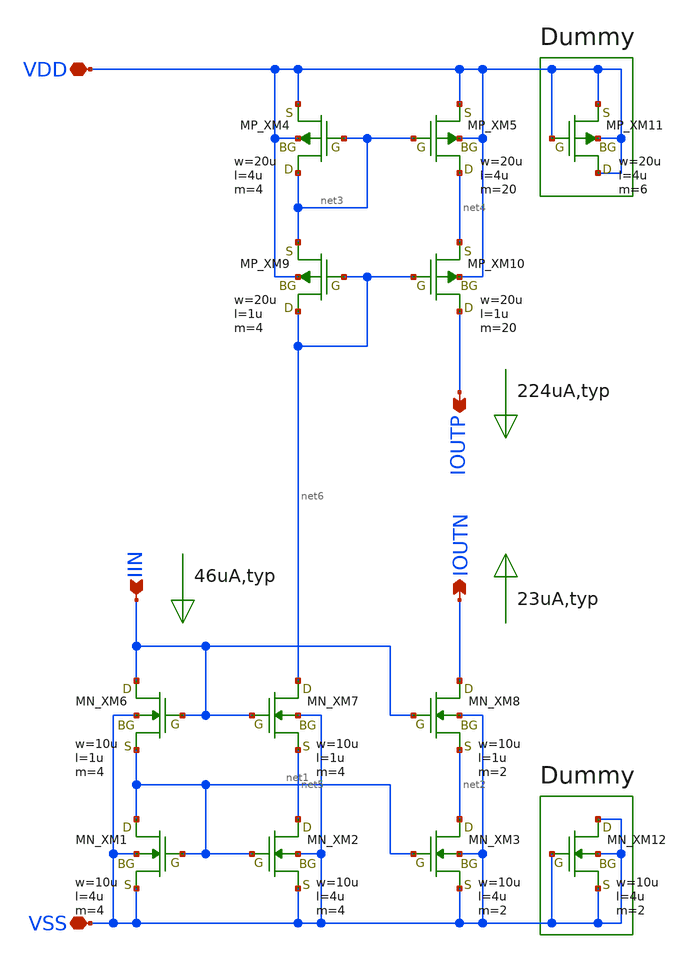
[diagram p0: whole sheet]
** sch_path: member_project/BGR/Maehashi/design/ibuf.sch
**.subckt ibuf VSS VDD IIN IOUTN IOUTP
*.iopin VSS
*.iopin VDD
*.ipin IIN
*.opin IOUTN
*.opin IOUTP
XXM1 net1 net1 VSS VSS NMOS w=10u l=4u as=0 ad=0 ps=0 pd=0 nrd=0 nrs=0 m=4
XXM2 net5 net1 VSS VSS NMOS w=10u l=4u as=0 ad=0 ps=0 pd=0 nrd=0 nrs=0 m=4
XXM3 net2 net1 VSS VSS NMOS w=10u l=4u as=0 ad=0 ps=0 pd=0 nrd=0 nrs=0 m=2
XXM4 net3 net3 VDD VDD PMOS w=20u l=4u as=0 ad=0 ps=0 pd=0 nrd=0 nrs=0 m=4
XXM5 net4 net3 VDD VDD PMOS w=20u l=4u as=0 ad=0 ps=0 pd=0 nrd=0 nrs=0 m=20
XXM6 IIN IIN net1 VSS NMOS w=10u l=1u as=0 ad=0 ps=0 pd=0 nrd=0 nrs=0 m=4
XXM7 net6 IIN net5 VSS NMOS w=10u l=1u as=0 ad=0 ps=0 pd=0 nrd=0 nrs=0 m=4
XXM8 IOUTN IIN net2 VSS NMOS w=10u l=1u as=0 ad=0 ps=0 pd=0 nrd=0 nrs=0 m=2
XXM9 net6 net6 net3 VDD PMOS w=20u l=1u as=0 ad=0 ps=0 pd=0 nrd=0 nrs=0 m=4
XXM10 IOUTP net6 net4 VDD PMOS w=20u l=1u as=0 ad=0 ps=0 pd=0 nrd=0 nrs=0 m=20
XXM11 VDD VDD VDD VDD PMOS w=20u l=4u as=0 ad=0 ps=0 pd=0 nrd=0 nrs=0 m=6
XXM12 VSS VSS VSS VSS NMOS w=10u l=4u as=0 ad=0 ps=0 pd=0 nrd=0 nrs=0 m=2
**.ends
.end
